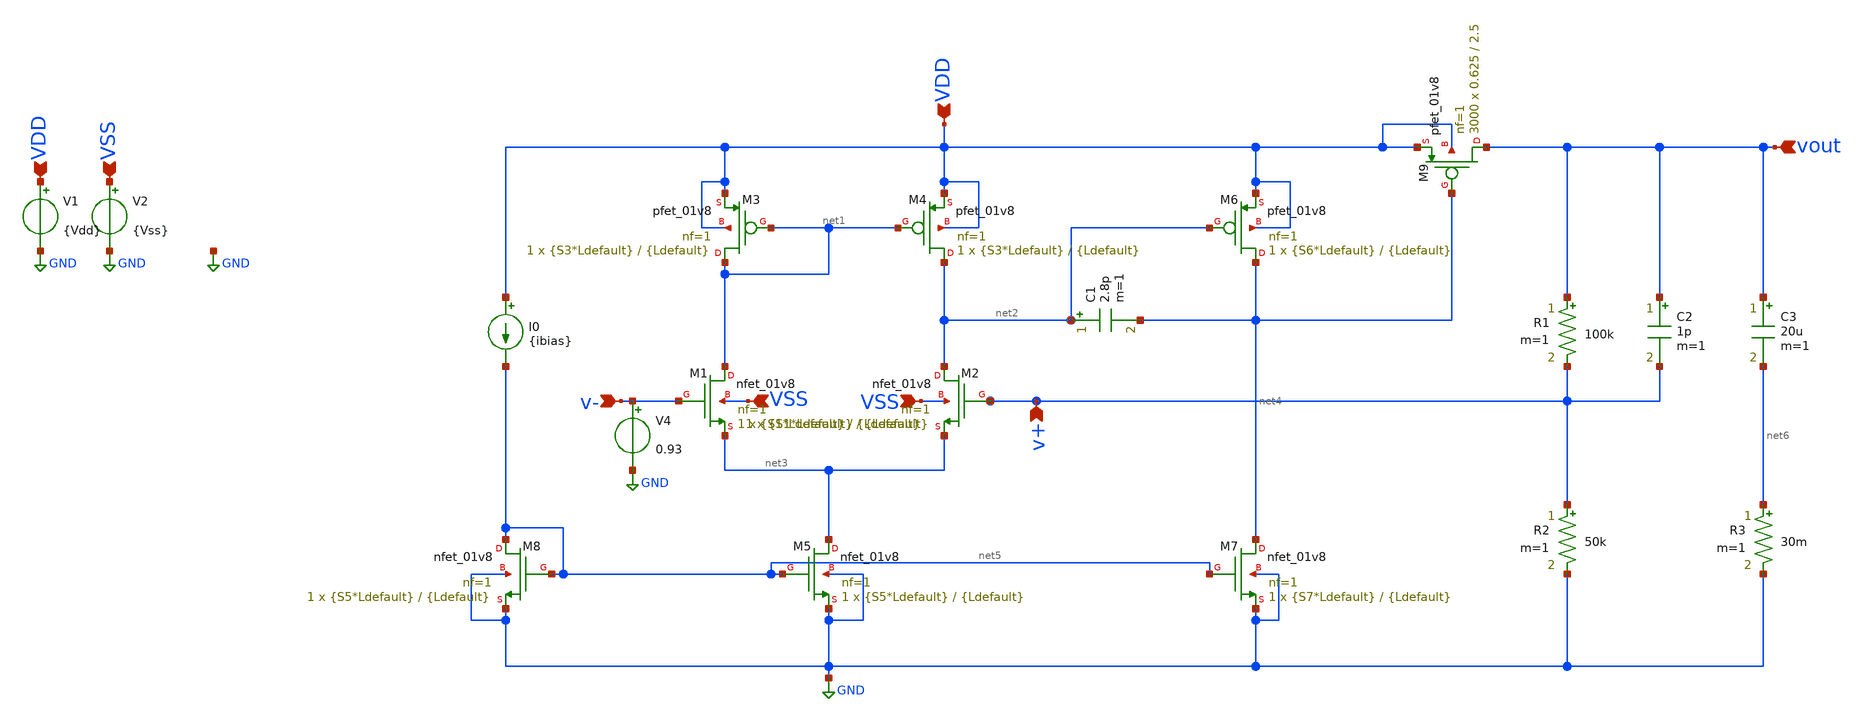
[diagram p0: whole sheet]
** sch_path: xschem/UREx-LDO-template.sch
**.subckt UREx-LDO-template VDD VSS VSS v- v+ vout VDD VSS
*.ipin VDD
*.ipin VSS
*.ipin VSS
*.ipin v-
*.ipin v+
*.ipin vout
*.ipin VDD
*.ipin VSS
XM1 net1 v- net3 VSS sky130_fd_pr__nfet_01v8 L={Ldefault} W={S1*Ldefault} nf=1 ad='int((1 + 1)/2) * {S1*Ldefault} / 1 * 0.29'
+ as='int((1 + 2)/2) * {S1*Ldefault} / 1 * 0.29' pd='2*int((1 + 1)/2) * ({S1*Ldefault} / 1 + 0.29)' ps='2*int((1 + 2)/2) * ({S1*Ldefault} / 1 + 0.29)'
+ nrd='0.29 / {S1*Ldefault} ' nrs='0.29 / {S1*Ldefault} ' sa=0 sb=0 sd=0 mult=1 m=1
XM3 net1 net1 VDD VDD sky130_fd_pr__pfet_01v8 L={Ldefault} W={S3*Ldefault} nf=1 ad='int((1 + 1)/2) * {S3*Ldefault} / 1 * 0.29'
+ as='int((1 + 2)/2) * {S3*Ldefault} / 1 * 0.29' pd='2*int((1 + 1)/2) * ({S3*Ldefault} / 1 + 0.29)' ps='2*int((1 + 2)/2) * ({S3*Ldefault} / 1 + 0.29)'
+ nrd='0.29 / {S3*Ldefault} ' nrs='0.29 / {S3*Ldefault} ' sa=0 sb=0 sd=0 mult=1 m=1
XM2 net2 v+ net3 VSS sky130_fd_pr__nfet_01v8 L={Ldefault} W={S1*Ldefault} nf=1 ad='int((1 + 1)/2) * {S1*Ldefault} / 1 * 0.29'
+ as='int((1 + 2)/2) * {S1*Ldefault} / 1 * 0.29' pd='2*int((1 + 1)/2) * ({S1*Ldefault} / 1 + 0.29)' ps='2*int((1 + 2)/2) * ({S1*Ldefault} / 1 + 0.29)'
+ nrd='0.29 / {S1*Ldefault} ' nrs='0.29 / {S1*Ldefault} ' sa=0 sb=0 sd=0 mult=1 m=1
XM4 net2 net1 VDD VDD sky130_fd_pr__pfet_01v8 L={Ldefault} W={S3*Ldefault} nf=1 ad='int((1 + 1)/2) * {S3*Ldefault} / 1 * 0.29'
+ as='int((1 + 2)/2) * {S3*Ldefault} / 1 * 0.29' pd='2*int((1 + 1)/2) * ({S3*Ldefault} / 1 + 0.29)' ps='2*int((1 + 2)/2) * ({S3*Ldefault} / 1 + 0.29)'
+ nrd='0.29 / {S3*Ldefault} ' nrs='0.29 / {S3*Ldefault} ' sa=0 sb=0 sd=0 mult=1 m=1
XM6 net4 net2 VDD VDD sky130_fd_pr__pfet_01v8 L={Ldefault} W={S6*Ldefault} nf=1 ad='int((1 + 1)/2) * {S6*Ldefault} / 1 * 0.29'
+ as='int((1 + 2)/2) * {S6*Ldefault} / 1 * 0.29' pd='2*int((1 + 1)/2) * ({S6*Ldefault} / 1 + 0.29)' ps='2*int((1 + 2)/2) * ({S6*Ldefault} / 1 + 0.29)'
+ nrd='0.29 / {S6*Ldefault} ' nrs='0.29 / {S6*Ldefault} ' sa=0 sb=0 sd=0 mult=1 m=1
XM5 net3 net5 GND GND sky130_fd_pr__nfet_01v8 L={Ldefault} W={S5*Ldefault} nf=1 ad='int((1 + 1)/2) * {S5*Ldefault} / 1 * 0.29'
+ as='int((1 + 2)/2) * {S5*Ldefault} / 1 * 0.29' pd='2*int((1 + 1)/2) * ({S5*Ldefault} / 1 + 0.29)' ps='2*int((1 + 2)/2) * ({S5*Ldefault} / 1 + 0.29)'
+ nrd='0.29 / {S5*Ldefault} ' nrs='0.29 / {S5*Ldefault} ' sa=0 sb=0 sd=0 mult=1 m=1
XM7 net4 net5 GND GND sky130_fd_pr__nfet_01v8 L={Ldefault} W={S7*Ldefault} nf=1 ad='int((1 + 1)/2) * {S7*Ldefault} / 1 * 0.29'
+ as='int((1 + 2)/2) * {S7*Ldefault} / 1 * 0.29' pd='2*int((1 + 1)/2) * ({S7*Ldefault} / 1 + 0.29)' ps='2*int((1 + 2)/2) * ({S7*Ldefault} / 1 + 0.29)'
+ nrd='0.29 / {S7*Ldefault} ' nrs='0.29 / {S7*Ldefault} ' sa=0 sb=0 sd=0 mult=1 m=1
XM8 net5 net5 GND GND sky130_fd_pr__nfet_01v8 L={Ldefault} W={S5*Ldefault} nf=1 ad='int((1 + 1)/2) * {S5*Ldefault} / 1 * 0.29'
+ as='int((1 + 2)/2) * {S5*Ldefault} / 1 * 0.29' pd='2*int((1 + 1)/2) * ({S5*Ldefault} / 1 + 0.29)' ps='2*int((1 + 2)/2) * ({S5*Ldefault} / 1 + 0.29)'
+ nrd='0.29 / {S5*Ldefault} ' nrs='0.29 / {S5*Ldefault} ' sa=0 sb=0 sd=0 mult=1 m=1
C1 net2 net4 2.8p m=1
V1 VDD GND {Vdd}
I0 VDD net5 {ibias}
V2 VSS GND {Vss}
R1 vout v+ 100k m=1
R2 v+ GND 50k m=1
V4 v- GND 0.93
XM9 vout net4 VDD VDD sky130_fd_pr__pfet_01v8 L=2.5 W=0.625 nf=1 ad='int((1 + 1)/2) * 0.625 / 1 * 0.29'
+ as='int((1 + 2)/2) * 0.625 / 1 * 0.29' pd='2*int((1 + 1)/2) * (0.625 / 1 + 0.29)' ps='2*int((1 + 2)/2) * (0.625 / 1 + 0.29)'
+ nrd='0.29 / 0.625 ' nrs='0.29 / 0.625 ' sa=0 sb=0 sd=0 mult=3000 m=3000
C2 vout v+ 1p m=1
C3 vout net6 20u m=1
R3 net6 GND 30m m=1
**** begin user architecture code



.lib /usr/local/share/pdk/sky130A/libs.tech/ngspice/sky130.lib.spice tt
.param Vdd=4 Vss=0 ibias=30u S1=4 S3=16 S5=8 S6=96 S7=32 Ldefault=0.25
.tran 5u 5m
*.ac dec 20 1 1e12
.save all

.control
run
*plot vout
*plot db(vout/v(v+))
*plot 180*cph(vout)/pi
set wr_singlescale
set wr_vecnames
*wrdata /foss/designs/2stageCMOSOpAmp/sim_data/GainvsFreq/gain(max).txt db(vout/v(v+))
*wrdata /foss/designs/2stageCMOSOpAmp/sim_data/sample_waves/a1.3m_f1k_gain700.txt vout
*wrdata /foss/designs/2stageCMOSOpAmp/sim_data/SR/SR.txt vout

.endc


**** end user architecture code
**.ends
.GLOBAL GND
.end
